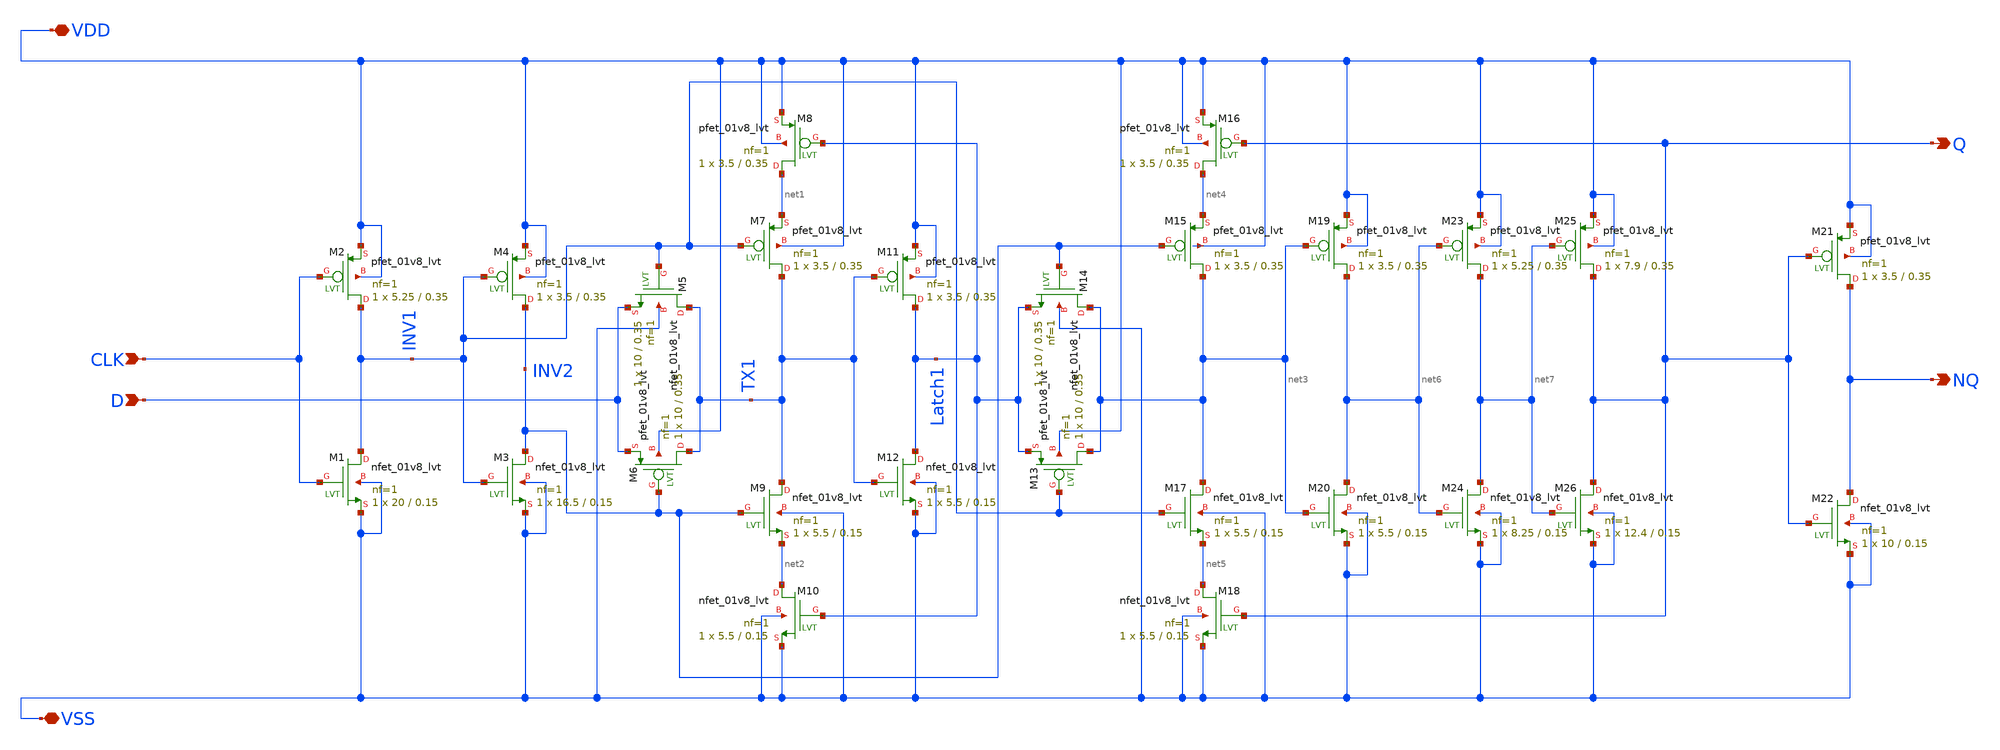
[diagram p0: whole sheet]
** sch_path: Circuits/lowpowerdflipflop2/xschem/lowpowerdflipflop2.sch
**.subckt lowpowerdflipflop2 D CLK Q NQ VSS VDD
*.ipin D
*.ipin CLK
*.opin Q
*.opin NQ
*.iopin VSS
*.iopin VDD
XM1 INV1 CLK VSS VSS sky130_fd_pr__nfet_01v8_lvt L=0.15 W=20 nf=1 ad='int((nf+1)/2) * W/nf * 0.29' as='int((nf+2)/2) * W/nf * 0.29'
+ pd='2*int((nf+1)/2) * (W/nf + 0.29)' ps='2*int((nf+2)/2) * (W/nf + 0.29)' nrd='0.29 / W' nrs='0.29 / W'
+ sa=0 sb=0 sd=0 mult=1 m=1
XM2 INV1 CLK VDD VDD sky130_fd_pr__pfet_01v8_lvt L=0.35 W=5.25 nf=1 ad='int((nf+1)/2) * W/nf * 0.29'
+ as='int((nf+2)/2) * W/nf * 0.29' pd='2*int((nf+1)/2) * (W/nf + 0.29)' ps='2*int((nf+2)/2) * (W/nf + 0.29)'
+ nrd='0.29 / W' nrs='0.29 / W' sa=0 sb=0 sd=0 mult=1 m=1
XM3 INV2 INV1 VSS VSS sky130_fd_pr__nfet_01v8_lvt L=0.15 W=16.5 nf=1 ad='int((nf+1)/2) * W/nf * 0.29'
+ as='int((nf+2)/2) * W/nf * 0.29' pd='2*int((nf+1)/2) * (W/nf + 0.29)' ps='2*int((nf+2)/2) * (W/nf + 0.29)'
+ nrd='0.29 / W' nrs='0.29 / W' sa=0 sb=0 sd=0 mult=1 m=1
XM4 INV2 INV1 VDD VDD sky130_fd_pr__pfet_01v8_lvt L=0.35 W=3.5 nf=1 ad='int((nf+1)/2) * W/nf * 0.29'
+ as='int((nf+2)/2) * W/nf * 0.29' pd='2*int((nf+1)/2) * (W/nf + 0.29)' ps='2*int((nf+2)/2) * (W/nf + 0.29)'
+ nrd='0.29 / W' nrs='0.29 / W' sa=0 sb=0 sd=0 mult=1 m=1
XM7 TX1 INV1 net1 VDD sky130_fd_pr__pfet_01v8_lvt L=0.35 W=3.5 nf=1 ad='int((nf+1)/2) * W/nf * 0.29'
+ as='int((nf+2)/2) * W/nf * 0.29' pd='2*int((nf+1)/2) * (W/nf + 0.29)' ps='2*int((nf+2)/2) * (W/nf + 0.29)'
+ nrd='0.29 / W' nrs='0.29 / W' sa=0 sb=0 sd=0 mult=1 m=1
XM8 net1 Latch1 VDD VDD sky130_fd_pr__pfet_01v8_lvt L=0.35 W=3.5 nf=1 ad='int((nf+1)/2) * W/nf * 0.29'
+ as='int((nf+2)/2) * W/nf * 0.29' pd='2*int((nf+1)/2) * (W/nf + 0.29)' ps='2*int((nf+2)/2) * (W/nf + 0.29)'
+ nrd='0.29 / W' nrs='0.29 / W' sa=0 sb=0 sd=0 mult=1 m=1
XM9 TX1 INV2 net2 VSS sky130_fd_pr__nfet_01v8_lvt L=0.15 W=5.5 nf=1 ad='int((nf+1)/2) * W/nf * 0.29'
+ as='int((nf+2)/2) * W/nf * 0.29' pd='2*int((nf+1)/2) * (W/nf + 0.29)' ps='2*int((nf+2)/2) * (W/nf + 0.29)'
+ nrd='0.29 / W' nrs='0.29 / W' sa=0 sb=0 sd=0 mult=1 m=1
XM10 net2 Latch1 VSS VSS sky130_fd_pr__nfet_01v8_lvt L=0.15 W=5.5 nf=1 ad='int((nf+1)/2) * W/nf * 0.29'
+ as='int((nf+2)/2) * W/nf * 0.29' pd='2*int((nf+1)/2) * (W/nf + 0.29)' ps='2*int((nf+2)/2) * (W/nf + 0.29)'
+ nrd='0.29 / W' nrs='0.29 / W' sa=0 sb=0 sd=0 mult=1 m=1
XM12 Latch1 TX1 VSS VSS sky130_fd_pr__nfet_01v8_lvt L=0.15 W=5.5 nf=1 ad='int((nf+1)/2) * W/nf * 0.29'
+ as='int((nf+2)/2) * W/nf * 0.29' pd='2*int((nf+1)/2) * (W/nf + 0.29)' ps='2*int((nf+2)/2) * (W/nf + 0.29)'
+ nrd='0.29 / W' nrs='0.29 / W' sa=0 sb=0 sd=0 mult=1 m=1
XM11 Latch1 TX1 VDD VDD sky130_fd_pr__pfet_01v8_lvt L=0.35 W=3.5 nf=1 ad='int((nf+1)/2) * W/nf * 0.29'
+ as='int((nf+2)/2) * W/nf * 0.29' pd='2*int((nf+1)/2) * (W/nf + 0.29)' ps='2*int((nf+2)/2) * (W/nf + 0.29)'
+ nrd='0.29 / W' nrs='0.29 / W' sa=0 sb=0 sd=0 mult=1 m=1
XM15 net3 INV2 net4 VDD sky130_fd_pr__pfet_01v8_lvt L=0.35 W=3.5 nf=1 ad='int((nf+1)/2) * W/nf * 0.29'
+ as='int((nf+2)/2) * W/nf * 0.29' pd='2*int((nf+1)/2) * (W/nf + 0.29)' ps='2*int((nf+2)/2) * (W/nf + 0.29)'
+ nrd='0.29 / W' nrs='0.29 / W' sa=0 sb=0 sd=0 mult=1 m=1
XM16 net4 Q VDD VDD sky130_fd_pr__pfet_01v8_lvt L=0.35 W=3.5 nf=1 ad='int((nf+1)/2) * W/nf * 0.29' as='int((nf+2)/2) * W/nf * 0.29'
+ pd='2*int((nf+1)/2) * (W/nf + 0.29)' ps='2*int((nf+2)/2) * (W/nf + 0.29)' nrd='0.29 / W' nrs='0.29 / W'
+ sa=0 sb=0 sd=0 mult=1 m=1
XM17 net3 INV1 net5 VSS sky130_fd_pr__nfet_01v8_lvt L=0.15 W=5.5 nf=1 ad='int((nf+1)/2) * W/nf * 0.29'
+ as='int((nf+2)/2) * W/nf * 0.29' pd='2*int((nf+1)/2) * (W/nf + 0.29)' ps='2*int((nf+2)/2) * (W/nf + 0.29)'
+ nrd='0.29 / W' nrs='0.29 / W' sa=0 sb=0 sd=0 mult=1 m=1
XM18 net5 Q VSS VSS sky130_fd_pr__nfet_01v8_lvt L=0.15 W=5.5 nf=1 ad='int((nf+1)/2) * W/nf * 0.29' as='int((nf+2)/2) * W/nf * 0.29'
+ pd='2*int((nf+1)/2) * (W/nf + 0.29)' ps='2*int((nf+2)/2) * (W/nf + 0.29)' nrd='0.29 / W' nrs='0.29 / W'
+ sa=0 sb=0 sd=0 mult=1 m=1
XM19 net6 net3 VDD VDD sky130_fd_pr__pfet_01v8_lvt L=0.35 W=3.5 nf=1 ad='int((nf+1)/2) * W/nf * 0.29'
+ as='int((nf+2)/2) * W/nf * 0.29' pd='2*int((nf+1)/2) * (W/nf + 0.29)' ps='2*int((nf+2)/2) * (W/nf + 0.29)'
+ nrd='0.29 / W' nrs='0.29 / W' sa=0 sb=0 sd=0 mult=1 m=1
XM20 net6 net3 VSS VSS sky130_fd_pr__nfet_01v8_lvt L=0.15 W=5.5 nf=1 ad='int((nf+1)/2) * W/nf * 0.29'
+ as='int((nf+2)/2) * W/nf * 0.29' pd='2*int((nf+1)/2) * (W/nf + 0.29)' ps='2*int((nf+2)/2) * (W/nf + 0.29)'
+ nrd='0.29 / W' nrs='0.29 / W' sa=0 sb=0 sd=0 mult=1 m=1
XM21 NQ Q VDD VDD sky130_fd_pr__pfet_01v8_lvt L=0.35 W=3.5 nf=1 ad='int((nf+1)/2) * W/nf * 0.29' as='int((nf+2)/2) * W/nf * 0.29'
+ pd='2*int((nf+1)/2) * (W/nf + 0.29)' ps='2*int((nf+2)/2) * (W/nf + 0.29)' nrd='0.29 / W' nrs='0.29 / W'
+ sa=0 sb=0 sd=0 mult=1 m=1
XM22 NQ Q VSS VSS sky130_fd_pr__nfet_01v8_lvt L=0.15 W=10 nf=1 ad='int((nf+1)/2) * W/nf * 0.29' as='int((nf+2)/2) * W/nf * 0.29'
+ pd='2*int((nf+1)/2) * (W/nf + 0.29)' ps='2*int((nf+2)/2) * (W/nf + 0.29)' nrd='0.29 / W' nrs='0.29 / W'
+ sa=0 sb=0 sd=0 mult=1 m=1
XM6 TX1 INV2 D VDD sky130_fd_pr__pfet_01v8_lvt L=0.35 W=10 nf=1 ad='int((nf+1)/2) * W/nf * 0.29' as='int((nf+2)/2) * W/nf * 0.29'
+ pd='2*int((nf+1)/2) * (W/nf + 0.29)' ps='2*int((nf+2)/2) * (W/nf + 0.29)' nrd='0.29 / W' nrs='0.29 / W'
+ sa=0 sb=0 sd=0 mult=1 m=1
XM5 TX1 INV1 D VSS sky130_fd_pr__nfet_01v8_lvt L=0.35 W=10 nf=1 ad='int((nf+1)/2) * W/nf * 0.29' as='int((nf+2)/2) * W/nf * 0.29'
+ pd='2*int((nf+1)/2) * (W/nf + 0.29)' ps='2*int((nf+2)/2) * (W/nf + 0.29)' nrd='0.29 / W' nrs='0.29 / W'
+ sa=0 sb=0 sd=0 mult=1 m=1
XM13 net3 INV1 Latch1 VDD sky130_fd_pr__pfet_01v8_lvt L=0.35 W=10 nf=1 ad='int((nf+1)/2) * W/nf * 0.29'
+ as='int((nf+2)/2) * W/nf * 0.29' pd='2*int((nf+1)/2) * (W/nf + 0.29)' ps='2*int((nf+2)/2) * (W/nf + 0.29)'
+ nrd='0.29 / W' nrs='0.29 / W' sa=0 sb=0 sd=0 mult=1 m=1
XM14 net3 INV2 Latch1 VSS sky130_fd_pr__nfet_01v8_lvt L=0.35 W=10 nf=1 ad='int((nf+1)/2) * W/nf * 0.29'
+ as='int((nf+2)/2) * W/nf * 0.29' pd='2*int((nf+1)/2) * (W/nf + 0.29)' ps='2*int((nf+2)/2) * (W/nf + 0.29)'
+ nrd='0.29 / W' nrs='0.29 / W' sa=0 sb=0 sd=0 mult=1 m=1
XM23 net7 net6 VDD VDD sky130_fd_pr__pfet_01v8_lvt L=0.35 W=5.25 nf=1 ad='int((nf+1)/2) * W/nf * 0.29'
+ as='int((nf+2)/2) * W/nf * 0.29' pd='2*int((nf+1)/2) * (W/nf + 0.29)' ps='2*int((nf+2)/2) * (W/nf + 0.29)'
+ nrd='0.29 / W' nrs='0.29 / W' sa=0 sb=0 sd=0 mult=1 m=1
XM24 net7 net6 VSS VSS sky130_fd_pr__nfet_01v8_lvt L=0.15 W=8.25 nf=1 ad='int((nf+1)/2) * W/nf * 0.29'
+ as='int((nf+2)/2) * W/nf * 0.29' pd='2*int((nf+1)/2) * (W/nf + 0.29)' ps='2*int((nf+2)/2) * (W/nf + 0.29)'
+ nrd='0.29 / W' nrs='0.29 / W' sa=0 sb=0 sd=0 mult=1 m=1
XM25 Q net7 VDD VDD sky130_fd_pr__pfet_01v8_lvt L=0.35 W=7.9 nf=1 ad='int((nf+1)/2) * W/nf * 0.29' as='int((nf+2)/2) * W/nf * 0.29'
+ pd='2*int((nf+1)/2) * (W/nf + 0.29)' ps='2*int((nf+2)/2) * (W/nf + 0.29)' nrd='0.29 / W' nrs='0.29 / W'
+ sa=0 sb=0 sd=0 mult=1 m=1
XM26 Q net7 VSS VSS sky130_fd_pr__nfet_01v8_lvt L=0.15 W=12.4 nf=1 ad='int((nf+1)/2) * W/nf * 0.29' as='int((nf+2)/2) * W/nf * 0.29'
+ pd='2*int((nf+1)/2) * (W/nf + 0.29)' ps='2*int((nf+2)/2) * (W/nf + 0.29)' nrd='0.29 / W' nrs='0.29 / W'
+ sa=0 sb=0 sd=0 mult=1 m=1
**.ends
.end
